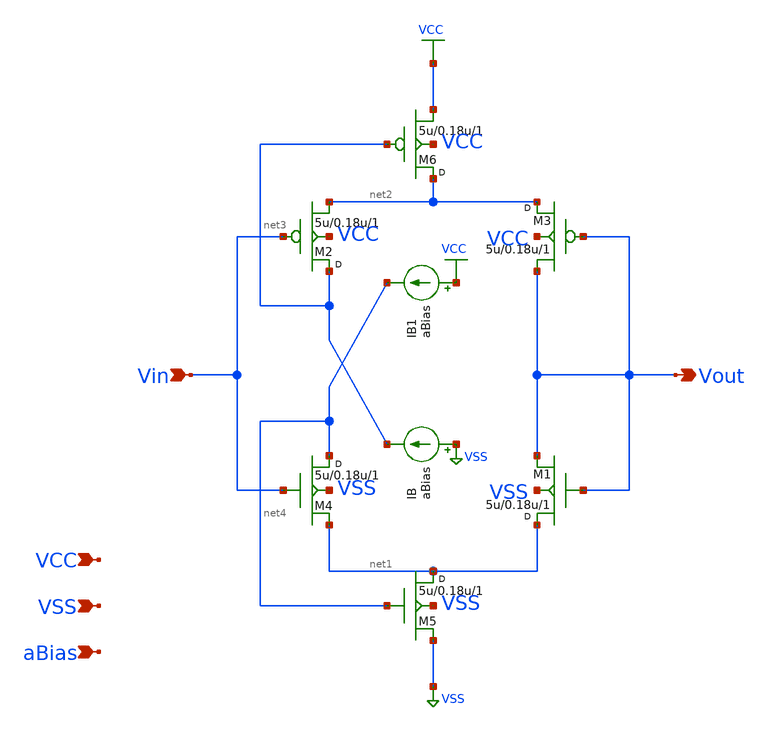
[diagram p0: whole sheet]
** sch_path: Voltage_Buffer.sch
**.subckt Voltage_Buffer Vin Vout VCC VSS aBias
*.ipin Vin
*.opin Vout
*.ipin VCC
*.ipin VSS
*.ipin aBias
M1 net1 Vout Vout VSS nmos w=5u l=0.18u m=1
M2 net3 Vin net2 VCC pmos w=5u l=0.18u m=1
M3 net2 Vout Vout VCC pmos w=5u l=0.18u m=1
M4 net4 Vin net1 VSS nmos w=5u l=0.18u m=1
M5 net1 net4 VSS VSS nmos w=5u l=0.18u m=1
M6 net2 net3 VCC VCC pmos w=5u l=0.18u m=1
IB VSS net3 aBias
IB1 VCC net4 aBias
**.ends
.GLOBAL VCC
.GLOBAL VSS
.end
